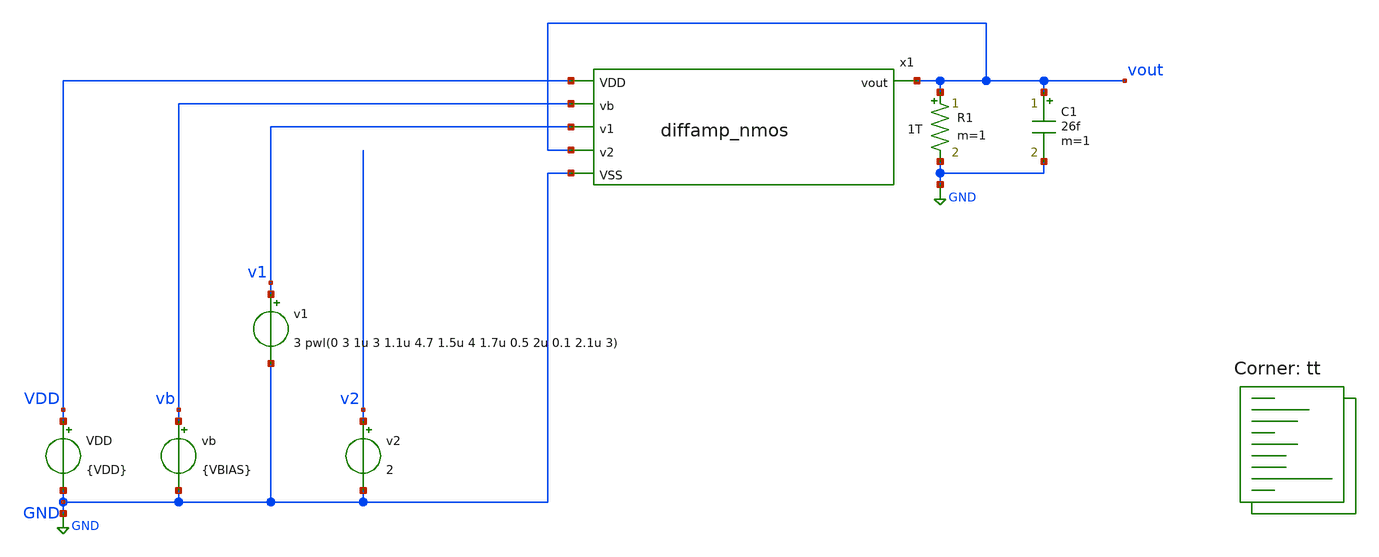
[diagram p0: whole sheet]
** sch_path: xschem/test_diffamp_nmos.sch
**.subckt test_diffamp_nmos
VDD VDD GND {VDD}
vb vb GND {VBIAS}
v1 v1 GND 3 pwl(0 3 1u 3 1.1u 4.7 1.5u 4 1.7u 0.5 2u 0.1 2.1u 3)
v2 v2 GND 2
R1 vout GND 1T m=1
x1 v1 vout GND VDD vb vout diffamp_nmos
C1 vout GND 26f m=1
**** begin user architecture code
.lib $::SKYWATER_MODELS/sky130.lib.spice tt



.options reltol=0.0001 abstol=10e-15
.include diffamp_nmos.spice
.param VDD=5
.param VSS=0
.param VBIAS=1
.options savecurrents
* .options reltol=0.01 abstol=10e-12
.control
  save all
  op
  remzerovec
  write test_diffamp_nmos.raw
  set appendwrite
  * vb sweep
  dc v1 0 6 0.2 vb 0 5 1
  remzerovec
  write test_diffamp_nmos.raw
  * dc sweep
  dc v1 0 5 0.1
  remzerovec
  write test_diffamp_nmos.raw
  * tran
  tran 1n 3u
  remzerovec
  write test_diffamp_nmos.raw
.endc



**** end user architecture code
**.ends
.GLOBAL GND
.end
